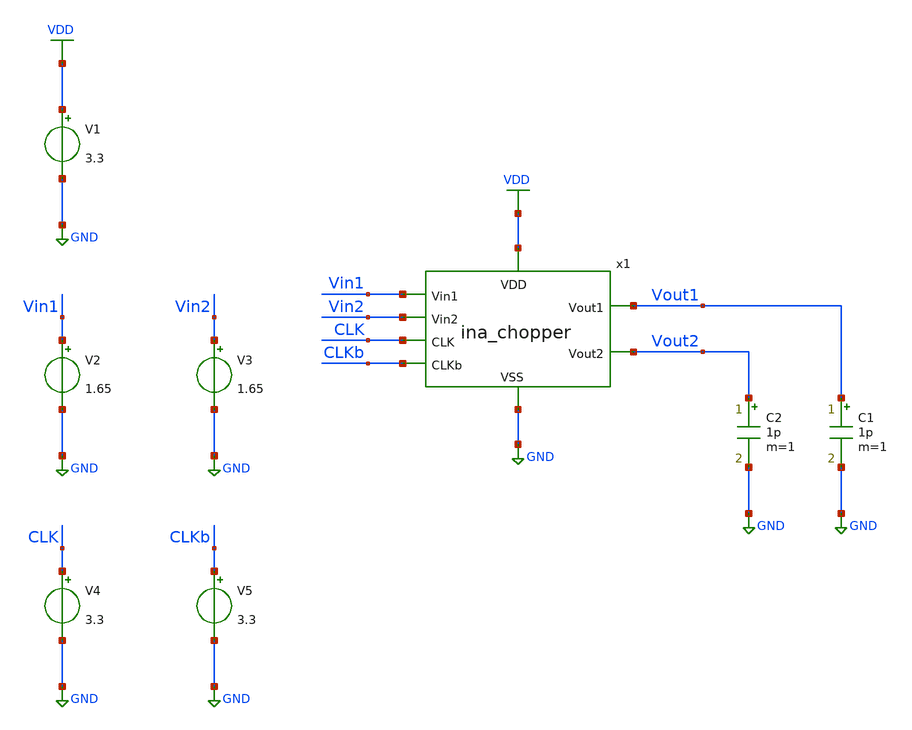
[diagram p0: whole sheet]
** sch_path: designs/libs/tb_ina/tb_ina_chopper_tran/tb_ina_chopper_tran.sch
**.subckt tb_ina_chopper_tran
V1 VDD GND 3.3
V2 Vin1 GND 1.65
V4 CLK GND 3.3
V5 CLKb GND 3.3
V3 Vin2 GND 1.65
C2 Vout2 GND 1p m=1
C1 Vout1 GND 1p m=1
x1 Vout2 Vin1 VDD GND CLKb CLK Vout1 Vin2 ina_chopper
**** begin user architecture code

.include $::180MCU_MODELS/design.ngspice
.lib $::180MCU_MODELS/sm141064.ngspice typical
.lib $::180MCU_MODELS/sm141064.ngspice cap_mim
.lib $::180MCU_MODELS/sm141064.ngspice moscap_typical
.lib $::180MCU_MODELS/sm141064.ngspice mimcap_typical
.lib $::180MCU_MODELS/sm141064.ngspice res_typical
* .lib $::180MCU_MODELS/sm141064.ngspice res_statistical
* ngspice commands




.control
save all

run
set color0 = white

*************************************
** ECG INPUT PARAMETERS
*************************************

let Vdd  = 3.3
let Vcm  = 1.65
let Vamp = 0.5m
let fecg = 100

*************************************
** CHOPPER PARAMETERS
*************************************

let fchop = 4k
let tper = 1/fchop
let td = 1u
let ton = tper/2-td
let tdclk = td/2
let tdclkb = tper/2+td/2
let tr = 10n
let tf = 10n

*************************************
** TRANSIENT PARAMETERS
*************************************

let tstop = 10m
let tstep = 100n

*************************************
** SOURCES
*************************************

alter @V1[DC] = $&Vdd
alter @V2[SIN] = [ $&Vcm $&Vamp $&fecg ]
alter @V3[SIN] = [ $&Vcm -$&Vamp $&fecg ]
alter @V4[PULSE] = [ 0 $&Vdd $&tdclk $&tr $&tf $&ton $&tper 0 ]
alter @V5[PULSE] = [ 0 $&Vdd $&tdclkb $&tr $&tf $&ton $&tper 0 ]

*************************************
** TRANSIENT SIMULATION
*************************************

tran $&tstep $&tstop

*************************************
** PLOTS
*************************************

setplot tran1
let vin_diff  = v(Vin1)-v(Vin2)
let vout_diff = v(Vout1)-v(Vout2)
let vin1 = v(Vin1)
let vin2 = v(Vin2)
let vout1 = v(Vout1)
let vout2 = v(Vout2)
let vclk = v(CLK)
let vclkb = v(CLKb)
plot vin_diff
plot vout_diff
plot vin1 vin2
plot vclk vclkb
plot vout1 vout2

*************************************
** SAVE
*************************************

write tb_ina_chopper_tran.raw


.endc
* ngspice commands



**** end user architecture code
**.ends

* expanding   symbol:  libs/core_ina/ina_chopper/ina_chopper.sym # of pins=8
** sym_path: designs/libs/core_ina/ina_chopper/ina_chopper.sym
** sch_path: designs/libs/core_ina/ina_chopper/ina_chopper.sch
.subckt ina_chopper Vout2 Vin1 VDD VSS CLKb CLK Vout1 Vin2
*.ipin Vin1
*.ipin Vin2
*.ipin CLKb
*.opin Vout2
*.ipin CLK
*.opin Vout1
*.ipin VDD
*.ipin VSS
XM1 Vout1 CLK Vin1 VSS nfet_03v3 L=0.28u W=5u nf=1 ad='int((nf+1)/2) * W/nf * 0.18u' as='int((nf+2)/2) * W/nf * 0.18u'
+ pd='2*int((nf+1)/2) * (W/nf + 0.18u)' ps='2*int((nf+2)/2) * (W/nf + 0.18u)' nrd='0.18u / W' nrs='0.18u / W'
+ sa=0 sb=0 sd=0 m=1
XM2 Vout1 CLKb Vin1 VDD pfet_03v3 L=0.28u W=10u nf=1 ad='int((nf+1)/2) * W/nf * 0.18u' as='int((nf+2)/2) * W/nf * 0.18u'
+ pd='2*int((nf+1)/2) * (W/nf + 0.18u)' ps='2*int((nf+2)/2) * (W/nf + 0.18u)' nrd='0.18u / W' nrs='0.18u / W'
+ sa=0 sb=0 sd=0 m=1
XM3 Vout2 CLKb Vin1 VSS nfet_03v3 L=0.28u W=5u nf=1 ad='int((nf+1)/2) * W/nf * 0.18u' as='int((nf+2)/2) * W/nf * 0.18u'
+ pd='2*int((nf+1)/2) * (W/nf + 0.18u)' ps='2*int((nf+2)/2) * (W/nf + 0.18u)' nrd='0.18u / W' nrs='0.18u / W'
+ sa=0 sb=0 sd=0 m=1
XM4 Vout2 CLK Vin1 VDD pfet_03v3 L=0.28u W=10u nf=1 ad='int((nf+1)/2) * W/nf * 0.18u' as='int((nf+2)/2) * W/nf * 0.18u'
+ pd='2*int((nf+1)/2) * (W/nf + 0.18u)' ps='2*int((nf+2)/2) * (W/nf + 0.18u)' nrd='0.18u / W' nrs='0.18u / W'
+ sa=0 sb=0 sd=0 m=1
XM5 Vin2 CLK Vout2 VSS nfet_03v3 L=0.28u W=5u nf=1 ad='int((nf+1)/2) * W/nf * 0.18u' as='int((nf+2)/2) * W/nf * 0.18u'
+ pd='2*int((nf+1)/2) * (W/nf + 0.18u)' ps='2*int((nf+2)/2) * (W/nf + 0.18u)' nrd='0.18u / W' nrs='0.18u / W'
+ sa=0 sb=0 sd=0 m=1
XM6 Vin2 CLKb Vout2 VDD pfet_03v3 L=0.28u W=10u nf=1 ad='int((nf+1)/2) * W/nf * 0.18u' as='int((nf+2)/2) * W/nf * 0.18u'
+ pd='2*int((nf+1)/2) * (W/nf + 0.18u)' ps='2*int((nf+2)/2) * (W/nf + 0.18u)' nrd='0.18u / W' nrs='0.18u / W'
+ sa=0 sb=0 sd=0 m=1
XM7 Vin2 CLKb Vout1 VSS nfet_03v3 L=0.28u W=5u nf=1 ad='int((nf+1)/2) * W/nf * 0.18u' as='int((nf+2)/2) * W/nf * 0.18u'
+ pd='2*int((nf+1)/2) * (W/nf + 0.18u)' ps='2*int((nf+2)/2) * (W/nf + 0.18u)' nrd='0.18u / W' nrs='0.18u / W'
+ sa=0 sb=0 sd=0 m=1
XM8 Vin2 CLK Vout1 VDD pfet_03v3 L=0.28u W=10u nf=1 ad='int((nf+1)/2) * W/nf * 0.18u' as='int((nf+2)/2) * W/nf * 0.18u'
+ pd='2*int((nf+1)/2) * (W/nf + 0.18u)' ps='2*int((nf+2)/2) * (W/nf + 0.18u)' nrd='0.18u / W' nrs='0.18u / W'
+ sa=0 sb=0 sd=0 m=1
.ends

.GLOBAL GND
.GLOBAL VDD
.end
